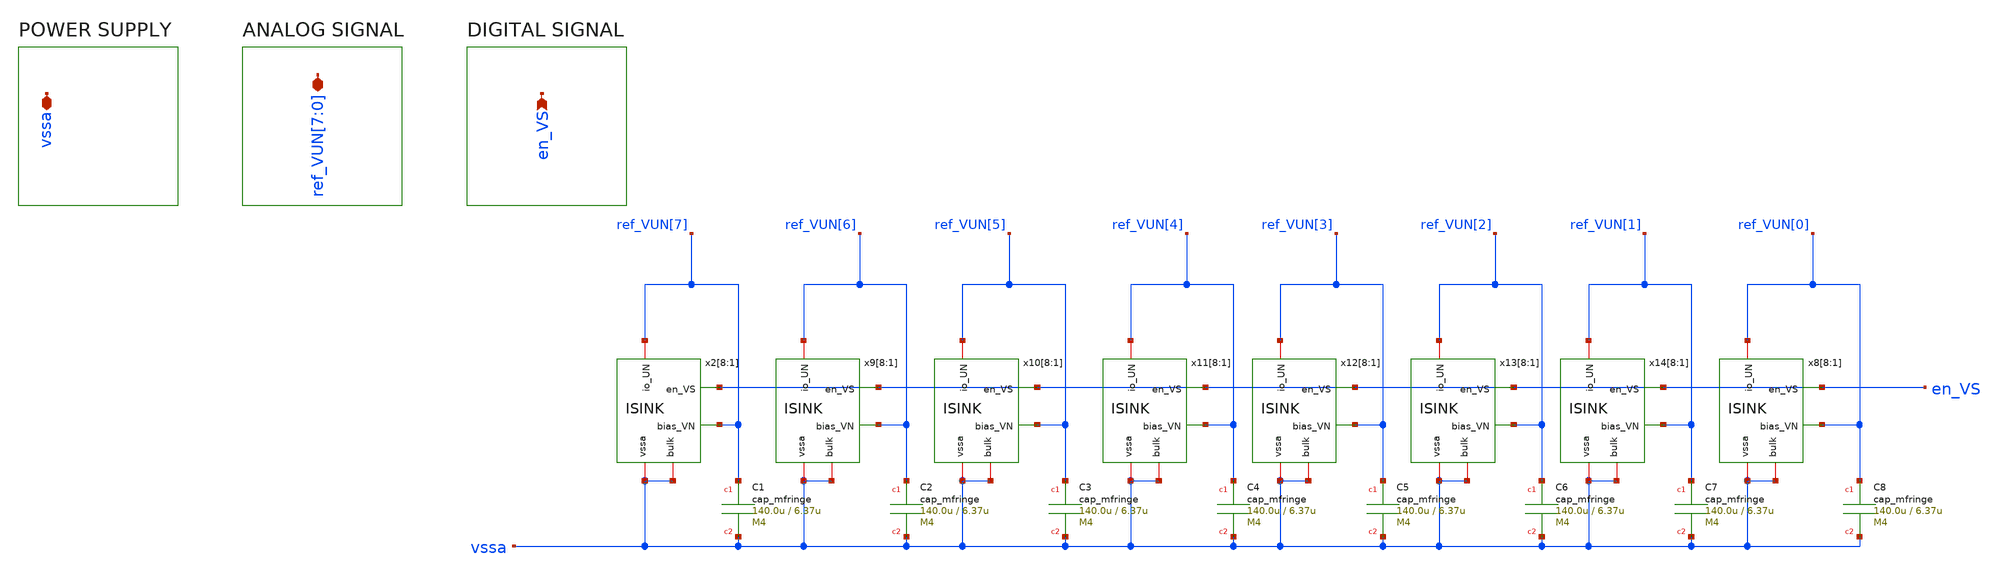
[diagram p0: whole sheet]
** sch_path: CoreDiodeT.sch
**.subckt CoreDiodeT
*+ ref_VUN[7],ref_VUN[6],ref_VUN[5],ref_VUN[4],ref_VUN[3],ref_VUN[2],ref_VUN[1],ref_VUN[0] en_VS vssa
*.iopin ref_VUN[7],ref_VUN[6],ref_VUN[5],ref_VUN[4],ref_VUN[3],ref_VUN[2],ref_VUN[1],ref_VUN[0]
*.ipin en_VS
*.iopin vssa
x2[8] ref_VUN[7] vssa en_VS ref_VUN[7] vssa ISINK
x2[7] ref_VUN[7] vssa en_VS ref_VUN[7] vssa ISINK
x2[6] ref_VUN[7] vssa en_VS ref_VUN[7] vssa ISINK
x2[5] ref_VUN[7] vssa en_VS ref_VUN[7] vssa ISINK
x2[4] ref_VUN[7] vssa en_VS ref_VUN[7] vssa ISINK
x2[3] ref_VUN[7] vssa en_VS ref_VUN[7] vssa ISINK
x2[2] ref_VUN[7] vssa en_VS ref_VUN[7] vssa ISINK
x2[1] ref_VUN[7] vssa en_VS ref_VUN[7] vssa ISINK
x9[8] ref_VUN[6] vssa en_VS ref_VUN[6] vssa ISINK
x9[7] ref_VUN[6] vssa en_VS ref_VUN[6] vssa ISINK
x9[6] ref_VUN[6] vssa en_VS ref_VUN[6] vssa ISINK
x9[5] ref_VUN[6] vssa en_VS ref_VUN[6] vssa ISINK
x9[4] ref_VUN[6] vssa en_VS ref_VUN[6] vssa ISINK
x9[3] ref_VUN[6] vssa en_VS ref_VUN[6] vssa ISINK
x9[2] ref_VUN[6] vssa en_VS ref_VUN[6] vssa ISINK
x9[1] ref_VUN[6] vssa en_VS ref_VUN[6] vssa ISINK
x10[8] ref_VUN[5] vssa en_VS ref_VUN[5] vssa ISINK
x10[7] ref_VUN[5] vssa en_VS ref_VUN[5] vssa ISINK
x10[6] ref_VUN[5] vssa en_VS ref_VUN[5] vssa ISINK
x10[5] ref_VUN[5] vssa en_VS ref_VUN[5] vssa ISINK
x10[4] ref_VUN[5] vssa en_VS ref_VUN[5] vssa ISINK
x10[3] ref_VUN[5] vssa en_VS ref_VUN[5] vssa ISINK
x10[2] ref_VUN[5] vssa en_VS ref_VUN[5] vssa ISINK
x10[1] ref_VUN[5] vssa en_VS ref_VUN[5] vssa ISINK
x11[8] ref_VUN[4] vssa en_VS ref_VUN[4] vssa ISINK
x11[7] ref_VUN[4] vssa en_VS ref_VUN[4] vssa ISINK
x11[6] ref_VUN[4] vssa en_VS ref_VUN[4] vssa ISINK
x11[5] ref_VUN[4] vssa en_VS ref_VUN[4] vssa ISINK
x11[4] ref_VUN[4] vssa en_VS ref_VUN[4] vssa ISINK
x11[3] ref_VUN[4] vssa en_VS ref_VUN[4] vssa ISINK
x11[2] ref_VUN[4] vssa en_VS ref_VUN[4] vssa ISINK
x11[1] ref_VUN[4] vssa en_VS ref_VUN[4] vssa ISINK
x12[8] ref_VUN[3] vssa en_VS ref_VUN[3] vssa ISINK
x12[7] ref_VUN[3] vssa en_VS ref_VUN[3] vssa ISINK
x12[6] ref_VUN[3] vssa en_VS ref_VUN[3] vssa ISINK
x12[5] ref_VUN[3] vssa en_VS ref_VUN[3] vssa ISINK
x12[4] ref_VUN[3] vssa en_VS ref_VUN[3] vssa ISINK
x12[3] ref_VUN[3] vssa en_VS ref_VUN[3] vssa ISINK
x12[2] ref_VUN[3] vssa en_VS ref_VUN[3] vssa ISINK
x12[1] ref_VUN[3] vssa en_VS ref_VUN[3] vssa ISINK
x13[8] ref_VUN[2] vssa en_VS ref_VUN[2] vssa ISINK
x13[7] ref_VUN[2] vssa en_VS ref_VUN[2] vssa ISINK
x13[6] ref_VUN[2] vssa en_VS ref_VUN[2] vssa ISINK
x13[5] ref_VUN[2] vssa en_VS ref_VUN[2] vssa ISINK
x13[4] ref_VUN[2] vssa en_VS ref_VUN[2] vssa ISINK
x13[3] ref_VUN[2] vssa en_VS ref_VUN[2] vssa ISINK
x13[2] ref_VUN[2] vssa en_VS ref_VUN[2] vssa ISINK
x13[1] ref_VUN[2] vssa en_VS ref_VUN[2] vssa ISINK
x14[8] ref_VUN[1] vssa en_VS ref_VUN[1] vssa ISINK
x14[7] ref_VUN[1] vssa en_VS ref_VUN[1] vssa ISINK
x14[6] ref_VUN[1] vssa en_VS ref_VUN[1] vssa ISINK
x14[5] ref_VUN[1] vssa en_VS ref_VUN[1] vssa ISINK
x14[4] ref_VUN[1] vssa en_VS ref_VUN[1] vssa ISINK
x14[3] ref_VUN[1] vssa en_VS ref_VUN[1] vssa ISINK
x14[2] ref_VUN[1] vssa en_VS ref_VUN[1] vssa ISINK
x14[1] ref_VUN[1] vssa en_VS ref_VUN[1] vssa ISINK
x8[8] ref_VUN[0] vssa en_VS ref_VUN[0] vssa ISINK
x8[7] ref_VUN[0] vssa en_VS ref_VUN[0] vssa ISINK
x8[6] ref_VUN[0] vssa en_VS ref_VUN[0] vssa ISINK
x8[5] ref_VUN[0] vssa en_VS ref_VUN[0] vssa ISINK
x8[4] ref_VUN[0] vssa en_VS ref_VUN[0] vssa ISINK
x8[3] ref_VUN[0] vssa en_VS ref_VUN[0] vssa ISINK
x8[2] ref_VUN[0] vssa en_VS ref_VUN[0] vssa ISINK
x8[1] ref_VUN[0] vssa en_VS ref_VUN[0] vssa ISINK
XC1 ref_VUN[7] vssa cap_mfringe w=140.0u l=6.37u mmin=1 mmax=4
XC2 ref_VUN[6] vssa cap_mfringe w=140.0u l=6.37u mmin=1 mmax=4
XC3 ref_VUN[5] vssa cap_mfringe w=140.0u l=6.37u mmin=1 mmax=4
XC4 ref_VUN[4] vssa cap_mfringe w=140.0u l=6.37u mmin=1 mmax=4
XC5 ref_VUN[3] vssa cap_mfringe w=140.0u l=6.37u mmin=1 mmax=4
XC6 ref_VUN[2] vssa cap_mfringe w=140.0u l=6.37u mmin=1 mmax=4
XC7 ref_VUN[1] vssa cap_mfringe w=140.0u l=6.37u mmin=1 mmax=4
XC8 ref_VUN[0] vssa cap_mfringe w=140.0u l=6.37u mmin=1 mmax=4
**.ends

* expanding   symbol:  ISINK.sym # of pins=5
** sym_path: ISINK.sym
** sch_path: ISINK.sch
.subckt ISINK bias_VN vssa en_VS io_UN bulk
*.ipin en_VS
*.iopin vssa
*.ipin bias_VN
*.iopin io_UN
*.iopin bulk
XM1 io_UN en_VS net2 bulk sg13_hv_nmos w=2.5u l=0.5u ng=1 m=1 mm_ok=1
XM2 net2 bias_VN net1 bulk sg13_hv_nmos w=1u l=4u ng=1 m=1 mm_ok=1
XM3 net1 bias_VN vssa bulk sg13_hv_nmos w=1u l=4u ng=1 m=1 mm_ok=1
.ends

.end
